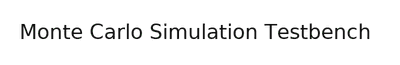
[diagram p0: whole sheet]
** sch_path: schemas/mc_testbench.sch
**.subckt mc_testbench
**** begin user architecture code

.option wnflag=1
.lib ~/skywater/skywater-pdk/libraries/sky130_fd_pr_ngspice/latest/models/sky130.lib.spice tt



.param W=32
.param L=4

.control
    set wr_singlescale
    let runs = 10
    let run = 1
    while run <= runs
        set appendwrite = FALSE
        set wr_vecnames
        let code = 0
        while code < 32
            if code eq 0
                let D0 = 0
            else
                let D0 = code % 2
            end
            if floor(code / 2 ) eq 0
                let D1 = 0
            else
                let D1 = floor(code / 2 ) % 2
            end
            if floor(code / 4 ) eq 0
                let D2 = 0
            else
                let D2 = floor(code / 4 ) % 2
            end
            if floor(code / 8 ) eq 0
                let D3 = 0
            else
                let D3 = floor(code / 8 ) % 2
            end

            alter VD0 $&D0
            alter VD1 $&D1
            alter VD2 $&D2
            alter VD3 $&D3

            save all
            op
            write ./data_fld/MCDACDATA{$&run}.csv v(D0) v(D1) v(D2) v(D3) i() v(V_out_final)
            if code eq 0
                set appendwrite
                set wr_vecnames = FALSE
            end
            let code = code + 1
        end
        reset
        let run = run + 1
    end
    quit
.endc

**** end user architecture code
**.ends
.end
